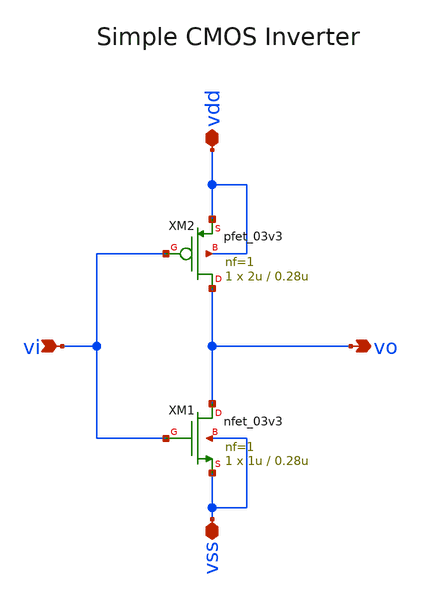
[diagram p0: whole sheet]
** sch_path: _build/images/iic-osic-tools/skel_eda/foss/examples/demo_gf180mcuD/ana/inv.sch
**.subckt inv vdd vss vi vo
*.iopin vdd
*.iopin vss
*.ipin vi
*.opin vo
XM1 vo vi vss vss nfet_03v3 L=0.28u W=1u nf=1 ad='int((nf+1)/2) * W/nf * 0.18u' as='int((nf+2)/2) * W/nf * 0.18u'
+ pd='2*int((nf+1)/2) * (W/nf + 0.18u)' ps='2*int((nf+2)/2) * (W/nf + 0.18u)' nrd='0.18u / W' nrs='0.18u / W'
+ sa=0 sb=0 sd=0 m=1
XM2 vo vi vdd vdd pfet_03v3 L=0.28u W=2u nf=1 ad='int((nf+1)/2) * W/nf * 0.18u' as='int((nf+2)/2) * W/nf * 0.18u'
+ pd='2*int((nf+1)/2) * (W/nf + 0.18u)' ps='2*int((nf+2)/2) * (W/nf + 0.18u)' nrd='0.18u / W' nrs='0.18u / W'
+ sa=0 sb=0 sd=0 m=1
**.ends
.end
